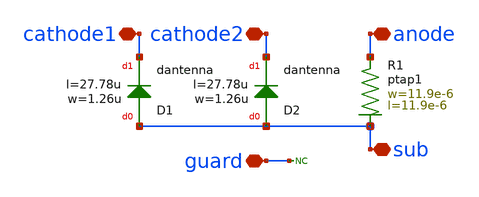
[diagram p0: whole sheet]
** sch_path: libs.tech/xschem/hm_stdcells/sg13g2_DCNDiode.sch
**.subckt sg13g2_DCNDiode cathode2 guard anode cathode1 sub
*.iopin cathode2
*.iopin guard
*.iopin anode
*.iopin cathode1
*.iopin sub
XR1 anode sub ptap1 R=5.179 w=11.9e-6 l=11.9e-6
XD1 sub cathode1 dantenna l=27.78u w=1.26u
* noconn guard
XD2 sub cathode2 dantenna l=27.78u w=1.26u
**.ends
.end
